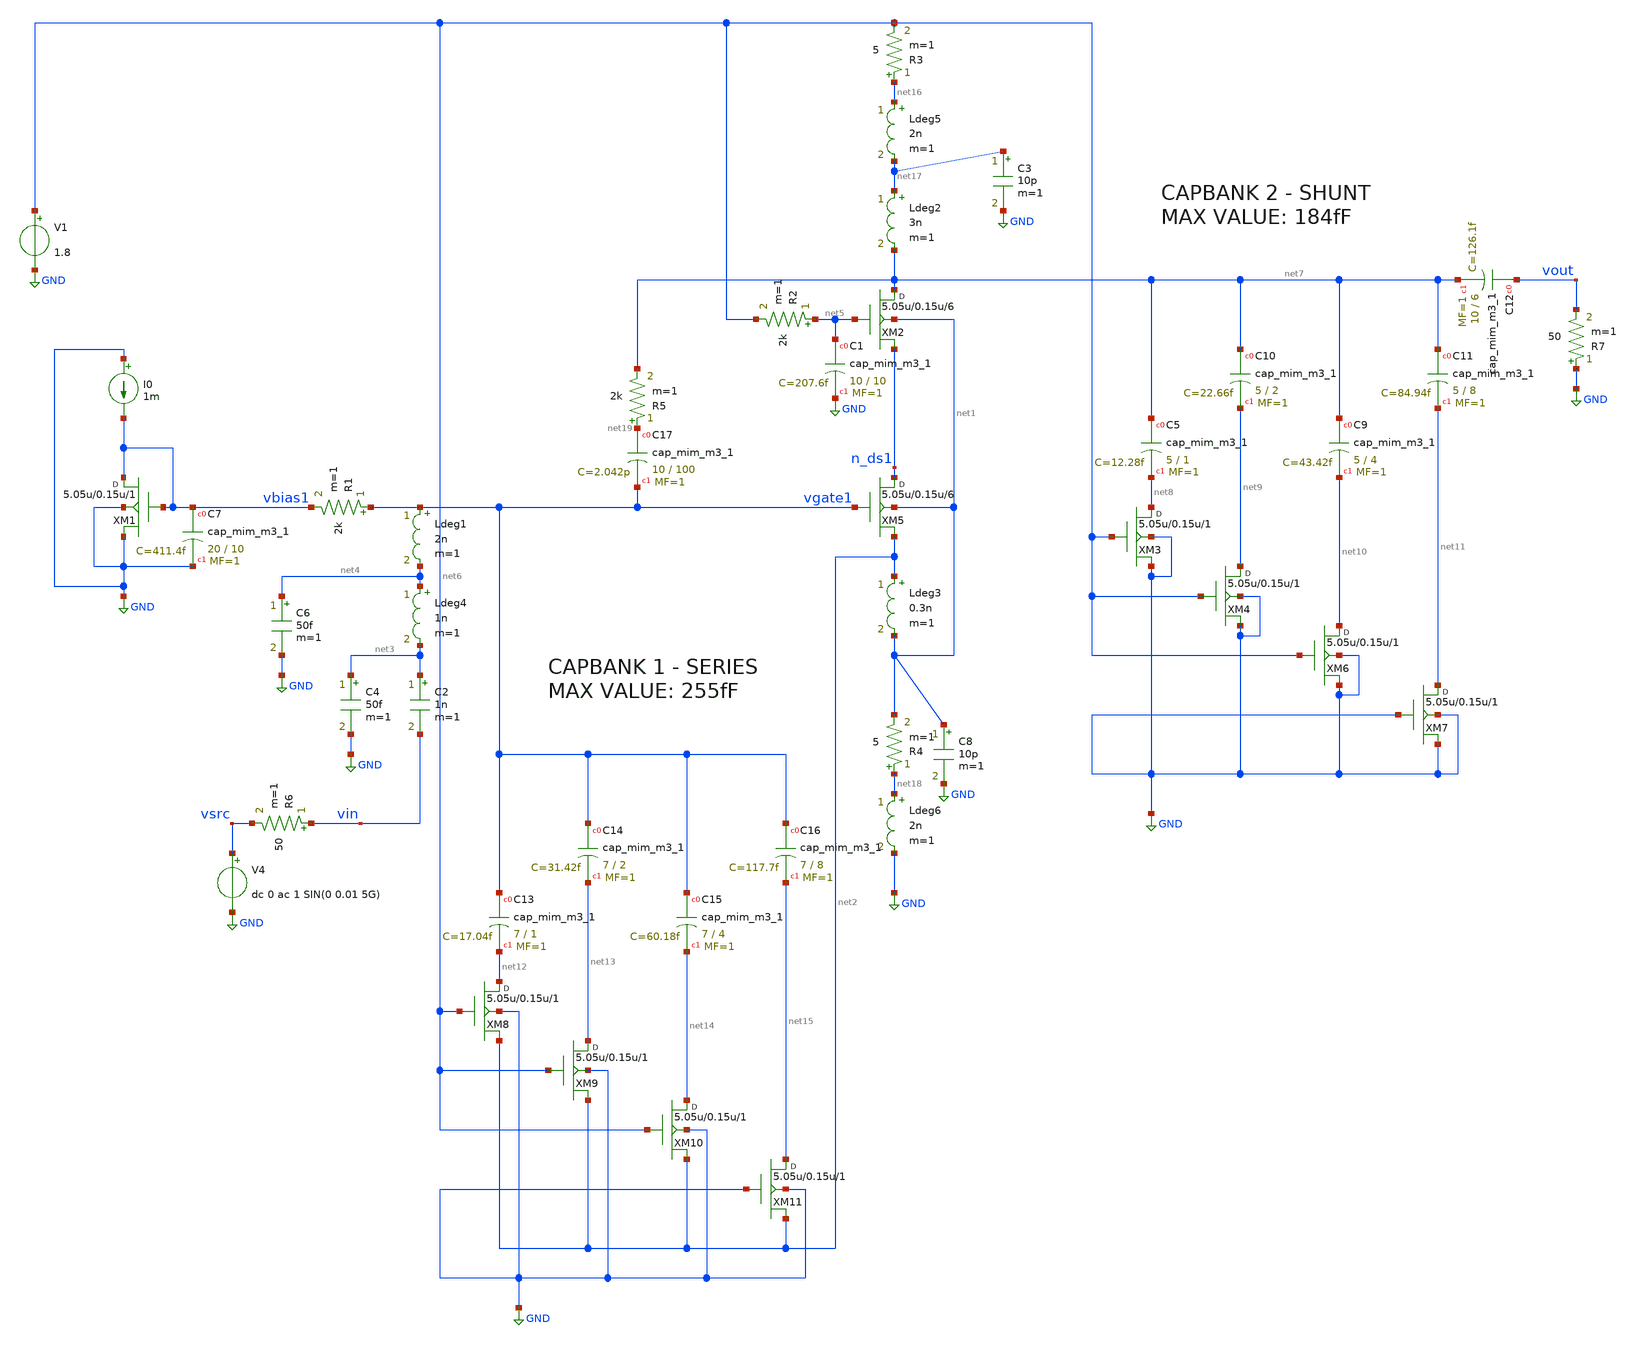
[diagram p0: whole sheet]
** sch_path: xschem/zptest_tran.sch
**.subckt zptest_tran
V1 net6 GND 1.8
Ldeg3 net2 net1 0.3n m=1
C2 net3 vin 1n m=1
R1 vgate1 vbias1 2k m=1
C4 net3 GND 50f m=1
Ldeg1 vgate1 net4 2n m=1
Ldeg4 net4 net3 1n m=1
C6 net4 GND 50f m=1
R2 net5 net6 2k m=1
I0 GND vbias1 1m
Ldeg2 net17 net7 3n m=1
XM5 n_ds1 vgate1 net2 net1 sky130_fd_pr__rf_nfet_01v8_bM04W5p00L0p15_ext w=5.05u l=0.15u m=6
XM1 vbias1 vbias1 GND GND sky130_fd_pr__rf_nfet_01v8_bM04W5p00L0p15_ext w=5.05u l=0.15u m=1
XM2 net7 net5 n_ds1 net1 sky130_fd_pr__rf_nfet_01v8_bM04W5p00L0p15_ext w=5.05u l=0.15u m=6
XC5 net7 net8 sky130_fd_pr__cap_mim_m3_1 W=5 L=1 MF=1 m=1
XC10 net7 net9 sky130_fd_pr__cap_mim_m3_1 W=5 L=2 MF=1 m=1
XC9 net7 net10 sky130_fd_pr__cap_mim_m3_1 W=5 L=4 MF=1 m=1
XC11 net7 net11 sky130_fd_pr__cap_mim_m3_1 W=5 L=8 MF=1 m=1
XM3 net8 net6 GND GND sky130_fd_pr__rf_nfet_01v8_bM04W5p00L0p15_ext w=5.05u l=0.15u m=1
XM4 net9 net6 GND GND sky130_fd_pr__rf_nfet_01v8_bM04W5p00L0p15_ext w=5.05u l=0.15u m=1
XM6 net10 net6 GND GND sky130_fd_pr__rf_nfet_01v8_bM04W5p00L0p15_ext w=5.05u l=0.15u m=1
XM7 net11 GND GND GND sky130_fd_pr__rf_nfet_01v8_bM04W5p00L0p15_ext w=5.05u l=0.15u m=1
XC12 vout net7 sky130_fd_pr__cap_mim_m3_1 W=10 L=6 MF=1 m=1
XC1 net5 GND sky130_fd_pr__cap_mim_m3_1 W=10 L=10 MF=1 m=1
XC7 vbias1 GND sky130_fd_pr__cap_mim_m3_1 W=20 L=10 MF=1 m=1
XC13 vgate1 net12 sky130_fd_pr__cap_mim_m3_1 W=7 L=1 MF=1 m=1
XC14 vgate1 net13 sky130_fd_pr__cap_mim_m3_1 W=7 L=2 MF=1 m=1
XC15 vgate1 net14 sky130_fd_pr__cap_mim_m3_1 W=7 L=4 MF=1 m=1
XC16 vgate1 net15 sky130_fd_pr__cap_mim_m3_1 W=7 L=8 MF=1 m=1
XM8 net12 net6 net2 GND sky130_fd_pr__rf_nfet_01v8_bM04W5p00L0p15_ext w=5.05u l=0.15u m=1
XM9 net13 net6 net2 GND sky130_fd_pr__rf_nfet_01v8_bM04W5p00L0p15_ext w=5.05u l=0.15u m=1
XM10 net14 net6 net2 GND sky130_fd_pr__rf_nfet_01v8_bM04W5p00L0p15_ext w=5.05u l=0.15u m=1
XM11 net15 GND net2 GND sky130_fd_pr__rf_nfet_01v8_bM04W5p00L0p15_ext w=5.05u l=0.15u m=1
Ldeg5 net16 net17 2n m=1
R3 net16 net6 5 m=1
C3 net17 GND 10p m=1
Ldeg6 net18 GND 2n m=1
R4 net18 net1 5 m=1
C8 net1 GND 10p m=1
R5 net19 net7 2k m=1
XC17 net19 vgate1 sky130_fd_pr__cap_mim_m3_1 W=10 L=100 MF=1 m=1
V4 vsrc GND dc 0 ac 1 SIN(0 0.01 5G)
R6 vin vsrc 50 m=1
R7 GND vout 50 m=1
**** begin user architecture code
.lib $::SKYWATER_MODELS/sky130.lib.spice tt
* .include $::PDKPATH/libs.ref/sky130_fd_sc_hvl/spice/sky130_fd_sc_hvl.spice



.subckt sky130_fd_pr__rf_nfet_01v8_bM04W5p00L0p15_ext DRAIN GATE SOURCE SUBSTRATE
X0 DRAIN GATE SOURCE SUBSTRATE sky130_fd_pr__nfet_01v8 ad=2.828e+12p pd=2.132e+07u as=4.242e+12p
+ ps=3.198e+07u w=5.05e+06u l=150000u
X1 SOURCE SUBSTRATE SUBSTRATE SUBSTRATE sky130_fd_pr__nfet_01v8 ad=0p pd=0u as=3.03e+12p
+ ps=2.14e+07u w=5.05e+06u l=150000u
X2 SOURCE GATE DRAIN SUBSTRATE sky130_fd_pr__nfet_01v8 ad=0p pd=0u as=0p ps=0u w=5.05e+06u l=150000u
X3 DRAIN GATE SOURCE SUBSTRATE sky130_fd_pr__nfet_01v8 ad=0p pd=0u as=0p ps=0u w=5.05e+06u l=150000u
X4 SUBSTRATE SUBSTRATE SOURCE SUBSTRATE sky130_fd_pr__nfet_01v8 ad=0p pd=0u as=0p ps=0u w=5.05e+06u
+ l=150000u
X5 SOURCE GATE DRAIN SUBSTRATE sky130_fd_pr__nfet_01v8 ad=0p pd=0u as=0p ps=0u w=5.05e+06u l=150000u
.ends
.tran 1ps 100ns
.control
run
display
plot vin
plot vout

.endc


**** end user architecture code
**.ends
.GLOBAL GND
.end
